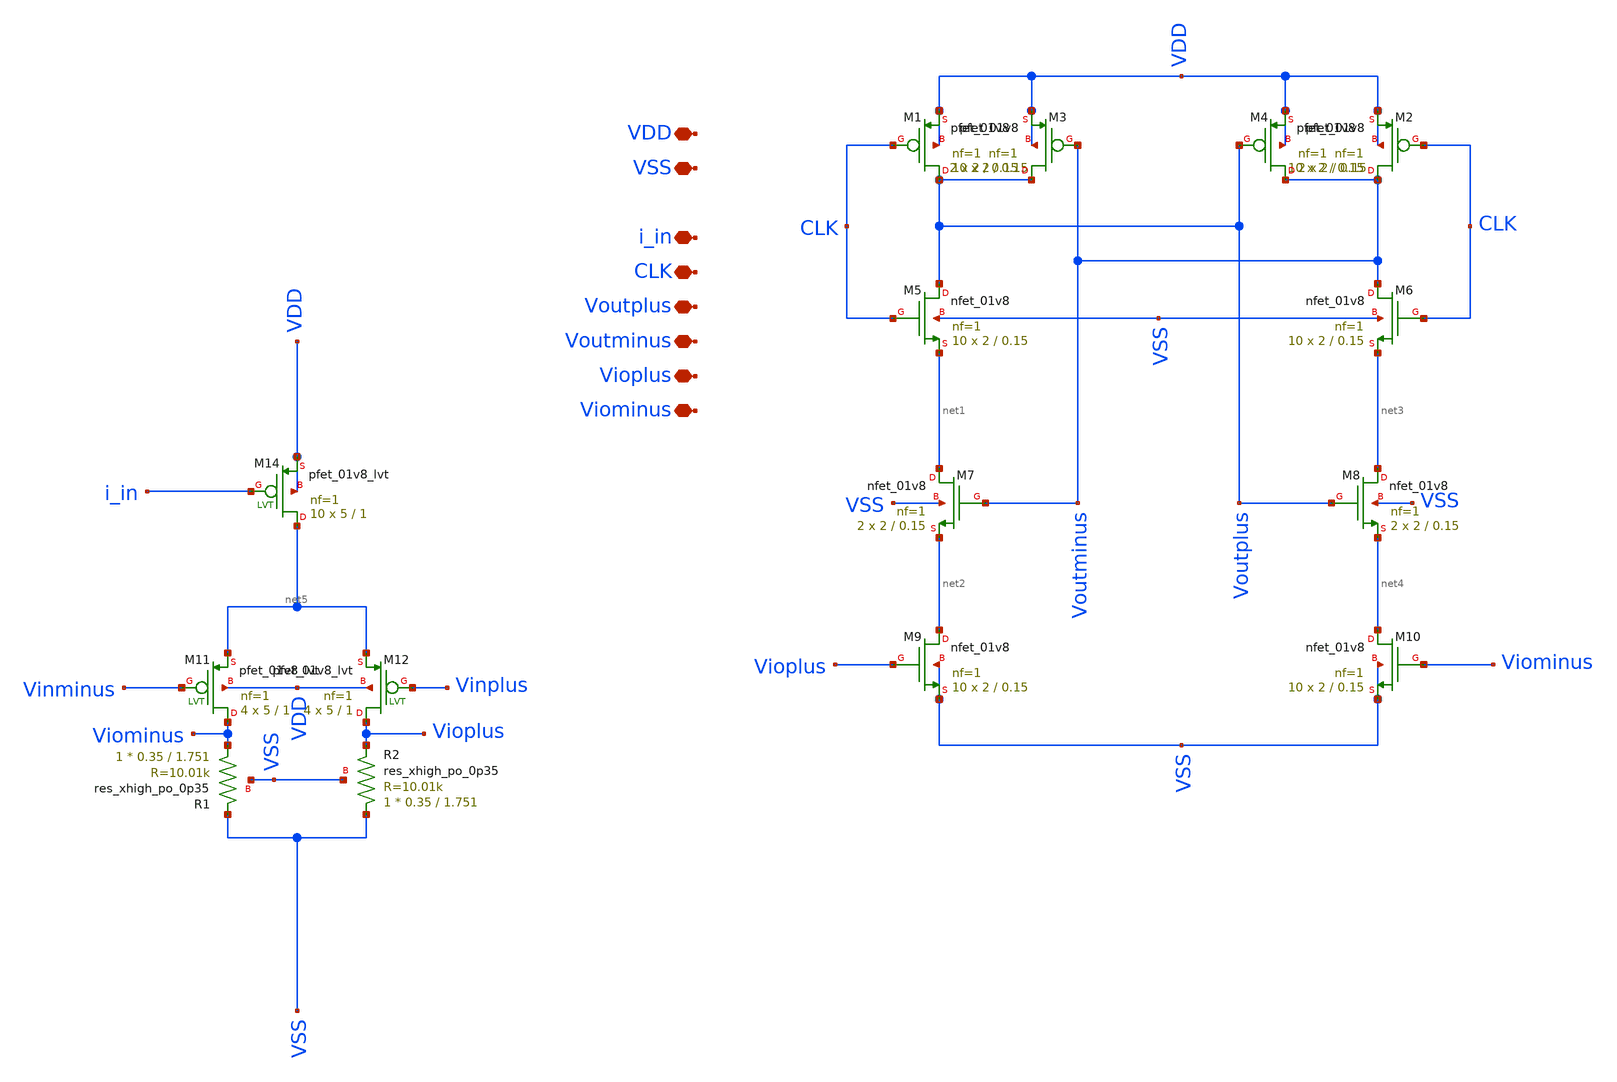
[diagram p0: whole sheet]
** sch_path: xschem/Comparator.sch
**.subckt Comparator VDD VSS CLK Voutplus Voutminus Vioplus Viominus i_in
*.iopin VDD
*.iopin VSS
*.iopin CLK
*.iopin Voutplus
*.iopin Voutminus
*.iopin Vioplus
*.iopin Viominus
*.iopin i_in
XM1 Voutplus CLK VDD VDD sky130_fd_pr__pfet_01v8 L=0.15 W=2 nf=1 ad='int((nf+1)/2) * W/nf * 0.29' as='int((nf+2)/2) * W/nf * 0.29'
+ pd='2*int((nf+1)/2) * (W/nf + 0.29)' ps='2*int((nf+2)/2) * (W/nf + 0.29)' nrd='0.29 / W' nrs='0.29 / W'
+ sa=0 sb=0 sd=0 mult=10 m=10
XM2 Voutminus CLK VDD VDD sky130_fd_pr__pfet_01v8 L=0.15 W=2 nf=1 ad='int((nf+1)/2) * W/nf * 0.29' as='int((nf+2)/2) * W/nf * 0.29'
+ pd='2*int((nf+1)/2) * (W/nf + 0.29)' ps='2*int((nf+2)/2) * (W/nf + 0.29)' nrd='0.29 / W' nrs='0.29 / W'
+ sa=0 sb=0 sd=0 mult=10 m=10
XM3 Voutplus Voutminus VDD VDD sky130_fd_pr__pfet_01v8 L=0.15 W=2 nf=1 ad='int((nf+1)/2) * W/nf * 0.29'
+ as='int((nf+2)/2) * W/nf * 0.29' pd='2*int((nf+1)/2) * (W/nf + 0.29)' ps='2*int((nf+2)/2) * (W/nf + 0.29)'
+ nrd='0.29 / W' nrs='0.29 / W' sa=0 sb=0 sd=0 mult=2 m=2
XM4 Voutminus Voutplus VDD VDD sky130_fd_pr__pfet_01v8 L=0.15 W=2 nf=1 ad='int((nf+1)/2) * W/nf * 0.29'
+ as='int((nf+2)/2) * W/nf * 0.29' pd='2*int((nf+1)/2) * (W/nf + 0.29)' ps='2*int((nf+2)/2) * (W/nf + 0.29)'
+ nrd='0.29 / W' nrs='0.29 / W' sa=0 sb=0 sd=0 mult=2 m=2
XM5 Voutplus CLK net1 VSS sky130_fd_pr__nfet_01v8 L=0.15 W=2 nf=1 ad='int((nf+1)/2) * W/nf * 0.29' as='int((nf+2)/2) * W/nf * 0.29'
+ pd='2*int((nf+1)/2) * (W/nf + 0.29)' ps='2*int((nf+2)/2) * (W/nf + 0.29)' nrd='0.29 / W' nrs='0.29 / W'
+ sa=0 sb=0 sd=0 mult=10 m=10
XM6 Voutminus CLK net3 VSS sky130_fd_pr__nfet_01v8 L=0.15 W=2 nf=1 ad='int((nf+1)/2) * W/nf * 0.29' as='int((nf+2)/2) * W/nf * 0.29'
+ pd='2*int((nf+1)/2) * (W/nf + 0.29)' ps='2*int((nf+2)/2) * (W/nf + 0.29)' nrd='0.29 / W' nrs='0.29 / W'
+ sa=0 sb=0 sd=0 mult=10 m=10
XM7 net1 Voutminus net2 VSS sky130_fd_pr__nfet_01v8 L=0.15 W=2 nf=1 ad='int((nf+1)/2) * W/nf * 0.29'
+ as='int((nf+2)/2) * W/nf * 0.29' pd='2*int((nf+1)/2) * (W/nf + 0.29)' ps='2*int((nf+2)/2) * (W/nf + 0.29)'
+ nrd='0.29 / W' nrs='0.29 / W' sa=0 sb=0 sd=0 mult=2 m=2
XM8 net3 Voutplus net4 VSS sky130_fd_pr__nfet_01v8 L=0.15 W=2 nf=1 ad='int((nf+1)/2) * W/nf * 0.29' as='int((nf+2)/2) * W/nf * 0.29'
+ pd='2*int((nf+1)/2) * (W/nf + 0.29)' ps='2*int((nf+2)/2) * (W/nf + 0.29)' nrd='0.29 / W' nrs='0.29 / W'
+ sa=0 sb=0 sd=0 mult=2 m=2
XM9 net2 Vioplus VSS VSS sky130_fd_pr__nfet_01v8 L=0.15 W=2 nf=1 ad='int((nf+1)/2) * W/nf * 0.29' as='int((nf+2)/2) * W/nf * 0.29'
+ pd='2*int((nf+1)/2) * (W/nf + 0.29)' ps='2*int((nf+2)/2) * (W/nf + 0.29)' nrd='0.29 / W' nrs='0.29 / W'
+ sa=0 sb=0 sd=0 mult=10 m=10
XM10 net4 Viominus VSS VSS sky130_fd_pr__nfet_01v8 L=0.15 W=2 nf=1 ad='int((nf+1)/2) * W/nf * 0.29' as='int((nf+2)/2) * W/nf * 0.29'
+ pd='2*int((nf+1)/2) * (W/nf + 0.29)' ps='2*int((nf+2)/2) * (W/nf + 0.29)' nrd='0.29 / W' nrs='0.29 / W'
+ sa=0 sb=0 sd=0 mult=10 m=10
XM11 Viominus Vinminus net5 VDD sky130_fd_pr__pfet_01v8_lvt L=1 W=5 nf=1 ad='int((nf+1)/2) * W/nf * 0.29'
+ as='int((nf+2)/2) * W/nf * 0.29' pd='2*int((nf+1)/2) * (W/nf + 0.29)' ps='2*int((nf+2)/2) * (W/nf + 0.29)'
+ nrd='0.29 / W' nrs='0.29 / W' sa=0 sb=0 sd=0 mult=4 m=4
XM12 Vioplus Vinplus net5 VDD sky130_fd_pr__pfet_01v8_lvt L=1 W=5 nf=1 ad='int((nf+1)/2) * W/nf * 0.29'
+ as='int((nf+2)/2) * W/nf * 0.29' pd='2*int((nf+1)/2) * (W/nf + 0.29)' ps='2*int((nf+2)/2) * (W/nf + 0.29)'
+ nrd='0.29 / W' nrs='0.29 / W' sa=0 sb=0 sd=0 mult=4 m=4
XM14 net5 i_in VDD VDD sky130_fd_pr__pfet_01v8_lvt L=1 W=5 nf=1 ad='int((nf+1)/2) * W/nf * 0.29' as='int((nf+2)/2) * W/nf * 0.29'
+ pd='2*int((nf+1)/2) * (W/nf + 0.29)' ps='2*int((nf+2)/2) * (W/nf + 0.29)' nrd='0.29 / W' nrs='0.29 / W'
+ sa=0 sb=0 sd=0 mult=10 m=10
XR2 VSS Vioplus VSS sky130_fd_pr__res_xhigh_po_0p35 L=1.751 mult=1 m=1
XR1 Viominus VSS VSS sky130_fd_pr__res_xhigh_po_0p35 L=1.751 mult=1 m=1
**.ends
.end
